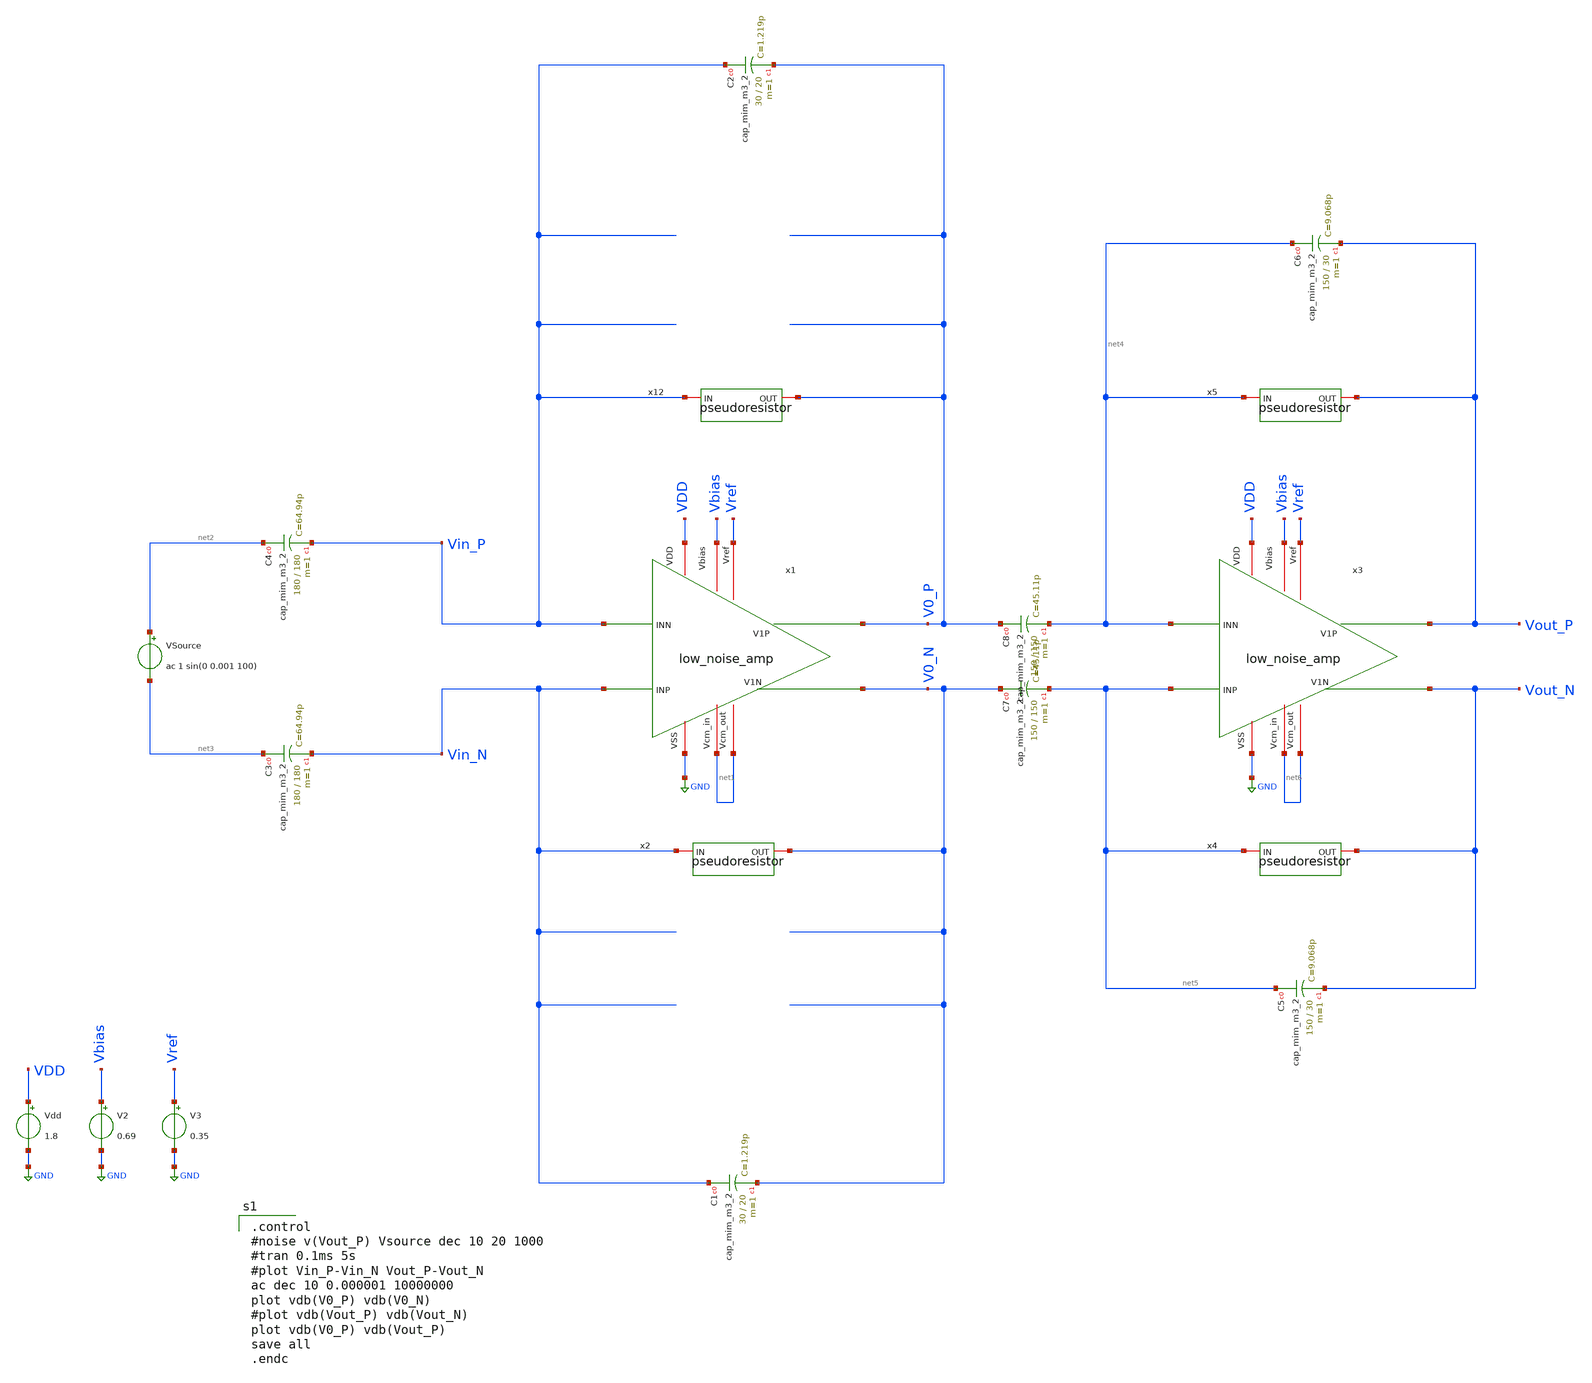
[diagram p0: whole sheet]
** sch_path: opamp_lna/low_noise_amp_tb_2.sch
**.subckt low_noise_amp_tb_2
x1 VDD net1 Vin_P Vin_N V0_P V0_N GND net1 Vbias Vref low_noise_amp
Vdd VDD GND 1.8
V2 Vbias GND 0.69
V3 Vref GND 0.35
VSource net2 net3 ac 1 sin(0 0.001 100)
x2 Vin_N V0_N pseudoresistor
XC1 Vin_N V0_N sky130_fd_pr__cap_mim_m3_2 W=30 L=20 MF=1 m=1
XC2 Vin_P V0_P sky130_fd_pr__cap_mim_m3_2 W=30 L=20 MF=1 m=1
XC3 net3 Vin_N sky130_fd_pr__cap_mim_m3_2 W=180 L=180 MF=1 m=1
XC4 net2 Vin_P sky130_fd_pr__cap_mim_m3_2 W=180 L=180 MF=1 m=1
x3 VDD net6 net4 net5 Vout_P Vout_N GND net6 Vbias Vref low_noise_amp
XC5 net5 Vout_N sky130_fd_pr__cap_mim_m3_2 W=150 L=30 MF=1 m=1
XC6 net4 Vout_P sky130_fd_pr__cap_mim_m3_2 W=150 L=30 MF=1 m=1
x12 Vin_P V0_P pseudoresistor
XC7 V0_N net5 sky130_fd_pr__cap_mim_m3_2 W=150 L=150 MF=1 m=1
XC8 V0_P net4 sky130_fd_pr__cap_mim_m3_2 W=150 L=150 MF=1 m=1
x4 net5 Vout_N pseudoresistor
x5 net4 Vout_P pseudoresistor
**** begin user architecture code

** opencircuitdesign pdks install
.lib $::SKYWATER_MODELS/sky130.lib.spice tt



.control
#noise v(Vout_P) Vsource dec 10 20 1000
#tran 0.1ms 5s
#plot Vin_P-Vin_N Vout_P-Vout_N
ac dec 10 0.000001 10000000
plot vdb(V0_P) vdb(V0_N)
#plot vdb(Vout_P) vdb(Vout_N)
plot vdb(V0_P) vdb(Vout_P)
save all
.endc

**** end user architecture code
**.ends

* expanding   symbol:  low_noise_amp.sym # of pins=10
** sym_path: opamp_lna/low_noise_amp.sym
** sch_path: opamp_lna/low_noise_amp.sch
.subckt low_noise_amp VDD Vcm_in INN INP V1P V1N VSS Vcm_out Vbias Vref
*.iopin VDD
*.iopin VSS
*.iopin Vbias
*.ipin INP
*.ipin INN
*.iopin Vref
*.iopin Vcm_in
*.iopin Vcm_out
*.opin V1N
*.opin V1P
XM3 CMFB Vref A0 VDD sky130_fd_pr__pfet_01v8 L=0.8 W=8 nf=1 ad='int((nf+1)/2) * W/nf * 0.29' as='int((nf+2)/2) * W/nf * 0.29'
+ pd='2*int((nf+1)/2) * (W/nf + 0.29)' ps='2*int((nf+2)/2) * (W/nf + 0.29)' nrd='0.29 / W' nrs='0.29 / W'
+ sa=0 sb=0 sd=0 mult=1 m=1
XM11 A0 Vbias VDD VDD sky130_fd_pr__pfet_01v8 L=0.8 W=4 nf=1 ad='int((nf+1)/2) * W/nf * 0.29' as='int((nf+2)/2) * W/nf * 0.29'
+ pd='2*int((nf+1)/2) * (W/nf + 0.29)' ps='2*int((nf+2)/2) * (W/nf + 0.29)' nrd='0.29 / W' nrs='0.29 / W'
+ sa=0 sb=0 sd=0 mult=1 m=1
XM7 V1N INP B0 VDD sky130_fd_pr__pfet_01v8 L=2 W=18 nf=1 ad='int((nf+1)/2) * W/nf * 0.29' as='int((nf+2)/2) * W/nf * 0.29'
+ pd='2*int((nf+1)/2) * (W/nf + 0.29)' ps='2*int((nf+2)/2) * (W/nf + 0.29)' nrd='0.29 / W' nrs='0.29 / W'
+ sa=0 sb=0 sd=0 mult=1 m=1
XM8 V1P INN B0 VDD sky130_fd_pr__pfet_01v8 L=2 W=18 nf=1 ad='int((nf+1)/2) * W/nf * 0.29' as='int((nf+2)/2) * W/nf * 0.29'
+ pd='2*int((nf+1)/2) * (W/nf + 0.29)' ps='2*int((nf+2)/2) * (W/nf + 0.29)' nrd='0.29 / W' nrs='0.29 / W'
+ sa=0 sb=0 sd=0 mult=1 m=1
XM9 V1N INP B1 VSS sky130_fd_pr__nfet_01v8 L=1 W=12 nf=1 ad='int((nf+1)/2) * W/nf * 0.29' as='int((nf+2)/2) * W/nf * 0.29'
+ pd='2*int((nf+1)/2) * (W/nf + 0.29)' ps='2*int((nf+2)/2) * (W/nf + 0.29)' nrd='0.29 / W' nrs='0.29 / W'
+ sa=0 sb=0 sd=0 mult=1 m=1
XM12 B0 Vbias VDD VDD sky130_fd_pr__pfet_01v8 L=0.8 W=4 nf=1 ad='int((nf+1)/2) * W/nf * 0.29' as='int((nf+2)/2) * W/nf * 0.29'
+ pd='2*int((nf+1)/2) * (W/nf + 0.29)' ps='2*int((nf+2)/2) * (W/nf + 0.29)' nrd='0.29 / W' nrs='0.29 / W'
+ sa=0 sb=0 sd=0 mult=1 m=1
XM13 B1 CMFB VSS VSS sky130_fd_pr__nfet_01v8 L=0.8 W=2 nf=1 ad='int((nf+1)/2) * W/nf * 0.29' as='int((nf+2)/2) * W/nf * 0.29'
+ pd='2*int((nf+1)/2) * (W/nf + 0.29)' ps='2*int((nf+2)/2) * (W/nf + 0.29)' nrd='0.29 / W' nrs='0.29 / W'
+ sa=0 sb=0 sd=0 mult=1 m=1
XM15 Vcm_out Vcm_out net1 Vcm_out sky130_fd_pr__pfet_01v8 L=0.6 W=1 nf=1 ad='int((nf+1)/2) * W/nf * 0.29'
+ as='int((nf+2)/2) * W/nf * 0.29' pd='2*int((nf+1)/2) * (W/nf + 0.29)' ps='2*int((nf+2)/2) * (W/nf + 0.29)'
+ nrd='0.29 / W' nrs='0.29 / W' sa=0 sb=0 sd=0 mult=5 m=5
XM16 net1 V1P V1P V1P sky130_fd_pr__pfet_01v8 L=0.6 W=1 nf=1 ad='int((nf+1)/2) * W/nf * 0.29' as='int((nf+2)/2) * W/nf * 0.29'
+ pd='2*int((nf+1)/2) * (W/nf + 0.29)' ps='2*int((nf+2)/2) * (W/nf + 0.29)' nrd='0.29 / W' nrs='0.29 / W'
+ sa=0 sb=0 sd=0 mult=5 m=5
XM17 Vcm_out Vcm_out net2 Vcm_out sky130_fd_pr__pfet_01v8 L=0.6 W=1 nf=1 ad='int((nf+1)/2) * W/nf * 0.29'
+ as='int((nf+2)/2) * W/nf * 0.29' pd='2*int((nf+1)/2) * (W/nf + 0.29)' ps='2*int((nf+2)/2) * (W/nf + 0.29)'
+ nrd='0.29 / W' nrs='0.29 / W' sa=0 sb=0 sd=0 mult=5 m=5
XM18 net2 V1N V1N V1N sky130_fd_pr__pfet_01v8 L=0.6 W=1 nf=1 ad='int((nf+1)/2) * W/nf * 0.29' as='int((nf+2)/2) * W/nf * 0.29'
+ pd='2*int((nf+1)/2) * (W/nf + 0.29)' ps='2*int((nf+2)/2) * (W/nf + 0.29)' nrd='0.29 / W' nrs='0.29 / W'
+ sa=0 sb=0 sd=0 mult=5 m=5
XC1 Vcm_out VSS sky130_fd_pr__cap_mim_m3_1 W=1 L=1 MF=1 m=1
XM1 V1P INN B1 VSS sky130_fd_pr__nfet_01v8 L=1 W=12 nf=1 ad='int((nf+1)/2) * W/nf * 0.29' as='int((nf+2)/2) * W/nf * 0.29'
+ pd='2*int((nf+1)/2) * (W/nf + 0.29)' ps='2*int((nf+2)/2) * (W/nf + 0.29)' nrd='0.29 / W' nrs='0.29 / W'
+ sa=0 sb=0 sd=0 mult=1 m=1
XM2 A1 A1 VSS VSS sky130_fd_pr__nfet_01v8 L=0.8 W=6 nf=1 ad='int((nf+1)/2) * W/nf * 0.29' as='int((nf+2)/2) * W/nf * 0.29'
+ pd='2*int((nf+1)/2) * (W/nf + 0.29)' ps='2*int((nf+2)/2) * (W/nf + 0.29)' nrd='0.29 / W' nrs='0.29 / W'
+ sa=0 sb=0 sd=0 mult=1 m=1
XM5 CMFB A1 VSS VSS sky130_fd_pr__nfet_01v8 L=0.8 W=6 nf=1 ad='int((nf+1)/2) * W/nf * 0.29' as='int((nf+2)/2) * W/nf * 0.29'
+ pd='2*int((nf+1)/2) * (W/nf + 0.29)' ps='2*int((nf+2)/2) * (W/nf + 0.29)' nrd='0.29 / W' nrs='0.29 / W'
+ sa=0 sb=0 sd=0 mult=1 m=1
XM6 A1 Vcm_in A0 VDD sky130_fd_pr__pfet_01v8 L=0.8 W=8 nf=1 ad='int((nf+1)/2) * W/nf * 0.29' as='int((nf+2)/2) * W/nf * 0.29'
+ pd='2*int((nf+1)/2) * (W/nf + 0.29)' ps='2*int((nf+2)/2) * (W/nf + 0.29)' nrd='0.29 / W' nrs='0.29 / W'
+ sa=0 sb=0 sd=0 mult=1 m=1
.ends


* expanding   symbol:  /home/lcg3895/CE393/pseudoresistor.sym # of pins=2
** sym_path: opamp_lna/pseudoresistor.sym
** sch_path: opamp_lna/pseudoresistor.sch
.subckt pseudoresistor IN OUT
*.iopin IN
*.iopin OUT
XM5 net1 IN IN IN sky130_fd_pr__pfet_01v8 L=0.5 W=1 nf=1 ad='int((nf+1)/2) * W/nf * 0.29' as='int((nf+2)/2) * W/nf * 0.29'
+ pd='2*int((nf+1)/2) * (W/nf + 0.29)' ps='2*int((nf+2)/2) * (W/nf + 0.29)' nrd='0.29 / W' nrs='0.29 / W'
+ sa=0 sb=0 sd=0 mult=10 m=10
XM1 net2 net2 net1 net2 sky130_fd_pr__pfet_01v8 L=0.5 W=1 nf=1 ad='int((nf+1)/2) * W/nf * 0.29' as='int((nf+2)/2) * W/nf * 0.29'
+ pd='2*int((nf+1)/2) * (W/nf + 0.29)' ps='2*int((nf+2)/2) * (W/nf + 0.29)' nrd='0.29 / W' nrs='0.29 / W'
+ sa=0 sb=0 sd=0 mult=10 m=10
XM2 net3 net2 net2 net2 sky130_fd_pr__pfet_01v8 L=0.5 W=1 nf=1 ad='int((nf+1)/2) * W/nf * 0.29' as='int((nf+2)/2) * W/nf * 0.29'
+ pd='2*int((nf+1)/2) * (W/nf + 0.29)' ps='2*int((nf+2)/2) * (W/nf + 0.29)' nrd='0.29 / W' nrs='0.29 / W'
+ sa=0 sb=0 sd=0 mult=10 m=10
XM3 OUT OUT net3 OUT sky130_fd_pr__pfet_01v8 L=0.5 W=1.2 nf=1 ad='int((nf+1)/2) * W/nf * 0.29' as='int((nf+2)/2) * W/nf * 0.29'
+ pd='2*int((nf+1)/2) * (W/nf + 0.29)' ps='2*int((nf+2)/2) * (W/nf + 0.29)' nrd='0.29 / W' nrs='0.29 / W'
+ sa=0 sb=0 sd=0 mult=1 m=1
.ends

.GLOBAL GND
.end
